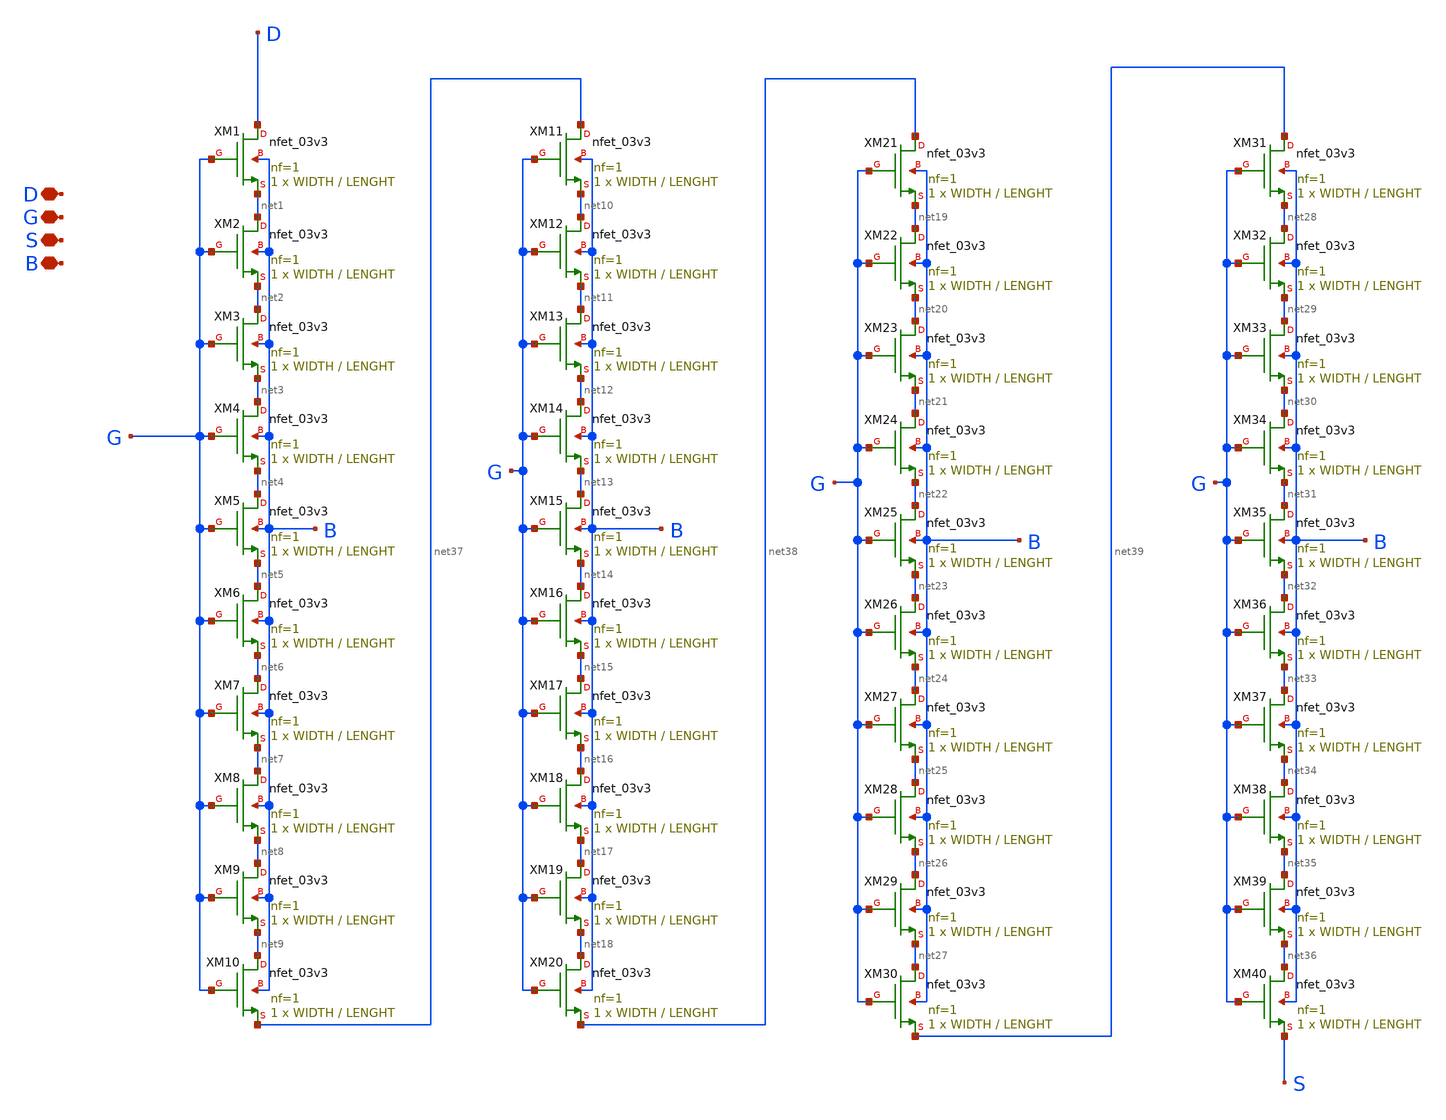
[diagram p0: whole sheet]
** sch_path: New_Extraction/Association/M4_ass.sch
**.subckt M4_ass D G S B
*.iopin D
*.iopin G
*.iopin S
*.iopin B
XM1 D G net1 B nfet_03v3 L=LENGHT W=WIDTH nf=1 ad='int((nf+1)/2) * W/nf * 0.18u' as='int((nf+2)/2) * W/nf * 0.18u'
+ pd='2*int((nf+1)/2) * (W/nf + 0.18u)' ps='2*int((nf+2)/2) * (W/nf + 0.18u)' nrd='0.18u / W' nrs='0.18u / W'
+ sa=0 sb=0 sd=0 m=1
XM2 net1 G net2 B nfet_03v3 L=LENGHT W=WIDTH nf=1 ad='int((nf+1)/2) * W/nf * 0.18u' as='int((nf+2)/2) * W/nf * 0.18u'
+ pd='2*int((nf+1)/2) * (W/nf + 0.18u)' ps='2*int((nf+2)/2) * (W/nf + 0.18u)' nrd='0.18u / W' nrs='0.18u / W'
+ sa=0 sb=0 sd=0 m=1
XM3 net2 G net3 B nfet_03v3 L=LENGHT W=WIDTH nf=1 ad='int((nf+1)/2) * W/nf * 0.18u' as='int((nf+2)/2) * W/nf * 0.18u'
+ pd='2*int((nf+1)/2) * (W/nf + 0.18u)' ps='2*int((nf+2)/2) * (W/nf + 0.18u)' nrd='0.18u / W' nrs='0.18u / W'
+ sa=0 sb=0 sd=0 m=1
XM4 net3 G net4 B nfet_03v3 L=LENGHT W=WIDTH nf=1 ad='int((nf+1)/2) * W/nf * 0.18u' as='int((nf+2)/2) * W/nf * 0.18u'
+ pd='2*int((nf+1)/2) * (W/nf + 0.18u)' ps='2*int((nf+2)/2) * (W/nf + 0.18u)' nrd='0.18u / W' nrs='0.18u / W'
+ sa=0 sb=0 sd=0 m=1
XM5 net4 G net5 B nfet_03v3 L=LENGHT W=WIDTH nf=1 ad='int((nf+1)/2) * W/nf * 0.18u' as='int((nf+2)/2) * W/nf * 0.18u'
+ pd='2*int((nf+1)/2) * (W/nf + 0.18u)' ps='2*int((nf+2)/2) * (W/nf + 0.18u)' nrd='0.18u / W' nrs='0.18u / W'
+ sa=0 sb=0 sd=0 m=1
XM6 net5 G net6 B nfet_03v3 L=LENGHT W=WIDTH nf=1 ad='int((nf+1)/2) * W/nf * 0.18u' as='int((nf+2)/2) * W/nf * 0.18u'
+ pd='2*int((nf+1)/2) * (W/nf + 0.18u)' ps='2*int((nf+2)/2) * (W/nf + 0.18u)' nrd='0.18u / W' nrs='0.18u / W'
+ sa=0 sb=0 sd=0 m=1
XM7 net6 G net7 B nfet_03v3 L=LENGHT W=WIDTH nf=1 ad='int((nf+1)/2) * W/nf * 0.18u' as='int((nf+2)/2) * W/nf * 0.18u'
+ pd='2*int((nf+1)/2) * (W/nf + 0.18u)' ps='2*int((nf+2)/2) * (W/nf + 0.18u)' nrd='0.18u / W' nrs='0.18u / W'
+ sa=0 sb=0 sd=0 m=1
XM8 net7 G net8 B nfet_03v3 L=LENGHT W=WIDTH nf=1 ad='int((nf+1)/2) * W/nf * 0.18u' as='int((nf+2)/2) * W/nf * 0.18u'
+ pd='2*int((nf+1)/2) * (W/nf + 0.18u)' ps='2*int((nf+2)/2) * (W/nf + 0.18u)' nrd='0.18u / W' nrs='0.18u / W'
+ sa=0 sb=0 sd=0 m=1
XM9 net8 G net9 B nfet_03v3 L=LENGHT W=WIDTH nf=1 ad='int((nf+1)/2) * W/nf * 0.18u' as='int((nf+2)/2) * W/nf * 0.18u'
+ pd='2*int((nf+1)/2) * (W/nf + 0.18u)' ps='2*int((nf+2)/2) * (W/nf + 0.18u)' nrd='0.18u / W' nrs='0.18u / W'
+ sa=0 sb=0 sd=0 m=1
XM10 net9 G net37 B nfet_03v3 L=LENGHT W=WIDTH nf=1 ad='int((nf+1)/2) * W/nf * 0.18u' as='int((nf+2)/2) * W/nf * 0.18u'
+ pd='2*int((nf+1)/2) * (W/nf + 0.18u)' ps='2*int((nf+2)/2) * (W/nf + 0.18u)' nrd='0.18u / W' nrs='0.18u / W'
+ sa=0 sb=0 sd=0 m=1
XM11 net37 G net10 B nfet_03v3 L=LENGHT W=WIDTH nf=1 ad='int((nf+1)/2) * W/nf * 0.18u' as='int((nf+2)/2) * W/nf * 0.18u'
+ pd='2*int((nf+1)/2) * (W/nf + 0.18u)' ps='2*int((nf+2)/2) * (W/nf + 0.18u)' nrd='0.18u / W' nrs='0.18u / W'
+ sa=0 sb=0 sd=0 m=1
XM12 net10 G net11 B nfet_03v3 L=LENGHT W=WIDTH nf=1 ad='int((nf+1)/2) * W/nf * 0.18u' as='int((nf+2)/2) * W/nf * 0.18u'
+ pd='2*int((nf+1)/2) * (W/nf + 0.18u)' ps='2*int((nf+2)/2) * (W/nf + 0.18u)' nrd='0.18u / W' nrs='0.18u / W'
+ sa=0 sb=0 sd=0 m=1
XM13 net11 G net12 B nfet_03v3 L=LENGHT W=WIDTH nf=1 ad='int((nf+1)/2) * W/nf * 0.18u' as='int((nf+2)/2) * W/nf * 0.18u'
+ pd='2*int((nf+1)/2) * (W/nf + 0.18u)' ps='2*int((nf+2)/2) * (W/nf + 0.18u)' nrd='0.18u / W' nrs='0.18u / W'
+ sa=0 sb=0 sd=0 m=1
XM14 net12 G net13 B nfet_03v3 L=LENGHT W=WIDTH nf=1 ad='int((nf+1)/2) * W/nf * 0.18u' as='int((nf+2)/2) * W/nf * 0.18u'
+ pd='2*int((nf+1)/2) * (W/nf + 0.18u)' ps='2*int((nf+2)/2) * (W/nf + 0.18u)' nrd='0.18u / W' nrs='0.18u / W'
+ sa=0 sb=0 sd=0 m=1
XM15 net13 G net14 B nfet_03v3 L=LENGHT W=WIDTH nf=1 ad='int((nf+1)/2) * W/nf * 0.18u' as='int((nf+2)/2) * W/nf * 0.18u'
+ pd='2*int((nf+1)/2) * (W/nf + 0.18u)' ps='2*int((nf+2)/2) * (W/nf + 0.18u)' nrd='0.18u / W' nrs='0.18u / W'
+ sa=0 sb=0 sd=0 m=1
XM16 net14 G net15 B nfet_03v3 L=LENGHT W=WIDTH nf=1 ad='int((nf+1)/2) * W/nf * 0.18u' as='int((nf+2)/2) * W/nf * 0.18u'
+ pd='2*int((nf+1)/2) * (W/nf + 0.18u)' ps='2*int((nf+2)/2) * (W/nf + 0.18u)' nrd='0.18u / W' nrs='0.18u / W'
+ sa=0 sb=0 sd=0 m=1
XM17 net15 G net16 B nfet_03v3 L=LENGHT W=WIDTH nf=1 ad='int((nf+1)/2) * W/nf * 0.18u' as='int((nf+2)/2) * W/nf * 0.18u'
+ pd='2*int((nf+1)/2) * (W/nf + 0.18u)' ps='2*int((nf+2)/2) * (W/nf + 0.18u)' nrd='0.18u / W' nrs='0.18u / W'
+ sa=0 sb=0 sd=0 m=1
XM18 net16 G net17 B nfet_03v3 L=LENGHT W=WIDTH nf=1 ad='int((nf+1)/2) * W/nf * 0.18u' as='int((nf+2)/2) * W/nf * 0.18u'
+ pd='2*int((nf+1)/2) * (W/nf + 0.18u)' ps='2*int((nf+2)/2) * (W/nf + 0.18u)' nrd='0.18u / W' nrs='0.18u / W'
+ sa=0 sb=0 sd=0 m=1
XM19 net17 G net18 B nfet_03v3 L=LENGHT W=WIDTH nf=1 ad='int((nf+1)/2) * W/nf * 0.18u' as='int((nf+2)/2) * W/nf * 0.18u'
+ pd='2*int((nf+1)/2) * (W/nf + 0.18u)' ps='2*int((nf+2)/2) * (W/nf + 0.18u)' nrd='0.18u / W' nrs='0.18u / W'
+ sa=0 sb=0 sd=0 m=1
XM20 net18 G net38 B nfet_03v3 L=LENGHT W=WIDTH nf=1 ad='int((nf+1)/2) * W/nf * 0.18u' as='int((nf+2)/2) * W/nf * 0.18u'
+ pd='2*int((nf+1)/2) * (W/nf + 0.18u)' ps='2*int((nf+2)/2) * (W/nf + 0.18u)' nrd='0.18u / W' nrs='0.18u / W'
+ sa=0 sb=0 sd=0 m=1
XM21 net38 G net19 B nfet_03v3 L=LENGHT W=WIDTH nf=1 ad='int((nf+1)/2) * W/nf * 0.18u' as='int((nf+2)/2) * W/nf * 0.18u'
+ pd='2*int((nf+1)/2) * (W/nf + 0.18u)' ps='2*int((nf+2)/2) * (W/nf + 0.18u)' nrd='0.18u / W' nrs='0.18u / W'
+ sa=0 sb=0 sd=0 m=1
XM22 net19 G net20 B nfet_03v3 L=LENGHT W=WIDTH nf=1 ad='int((nf+1)/2) * W/nf * 0.18u' as='int((nf+2)/2) * W/nf * 0.18u'
+ pd='2*int((nf+1)/2) * (W/nf + 0.18u)' ps='2*int((nf+2)/2) * (W/nf + 0.18u)' nrd='0.18u / W' nrs='0.18u / W'
+ sa=0 sb=0 sd=0 m=1
XM23 net20 G net21 B nfet_03v3 L=LENGHT W=WIDTH nf=1 ad='int((nf+1)/2) * W/nf * 0.18u' as='int((nf+2)/2) * W/nf * 0.18u'
+ pd='2*int((nf+1)/2) * (W/nf + 0.18u)' ps='2*int((nf+2)/2) * (W/nf + 0.18u)' nrd='0.18u / W' nrs='0.18u / W'
+ sa=0 sb=0 sd=0 m=1
XM24 net21 G net22 B nfet_03v3 L=LENGHT W=WIDTH nf=1 ad='int((nf+1)/2) * W/nf * 0.18u' as='int((nf+2)/2) * W/nf * 0.18u'
+ pd='2*int((nf+1)/2) * (W/nf + 0.18u)' ps='2*int((nf+2)/2) * (W/nf + 0.18u)' nrd='0.18u / W' nrs='0.18u / W'
+ sa=0 sb=0 sd=0 m=1
XM25 net22 G net23 B nfet_03v3 L=LENGHT W=WIDTH nf=1 ad='int((nf+1)/2) * W/nf * 0.18u' as='int((nf+2)/2) * W/nf * 0.18u'
+ pd='2*int((nf+1)/2) * (W/nf + 0.18u)' ps='2*int((nf+2)/2) * (W/nf + 0.18u)' nrd='0.18u / W' nrs='0.18u / W'
+ sa=0 sb=0 sd=0 m=1
XM26 net23 G net24 B nfet_03v3 L=LENGHT W=WIDTH nf=1 ad='int((nf+1)/2) * W/nf * 0.18u' as='int((nf+2)/2) * W/nf * 0.18u'
+ pd='2*int((nf+1)/2) * (W/nf + 0.18u)' ps='2*int((nf+2)/2) * (W/nf + 0.18u)' nrd='0.18u / W' nrs='0.18u / W'
+ sa=0 sb=0 sd=0 m=1
XM27 net24 G net25 B nfet_03v3 L=LENGHT W=WIDTH nf=1 ad='int((nf+1)/2) * W/nf * 0.18u' as='int((nf+2)/2) * W/nf * 0.18u'
+ pd='2*int((nf+1)/2) * (W/nf + 0.18u)' ps='2*int((nf+2)/2) * (W/nf + 0.18u)' nrd='0.18u / W' nrs='0.18u / W'
+ sa=0 sb=0 sd=0 m=1
XM28 net25 G net26 B nfet_03v3 L=LENGHT W=WIDTH nf=1 ad='int((nf+1)/2) * W/nf * 0.18u' as='int((nf+2)/2) * W/nf * 0.18u'
+ pd='2*int((nf+1)/2) * (W/nf + 0.18u)' ps='2*int((nf+2)/2) * (W/nf + 0.18u)' nrd='0.18u / W' nrs='0.18u / W'
+ sa=0 sb=0 sd=0 m=1
XM29 net26 G net27 B nfet_03v3 L=LENGHT W=WIDTH nf=1 ad='int((nf+1)/2) * W/nf * 0.18u' as='int((nf+2)/2) * W/nf * 0.18u'
+ pd='2*int((nf+1)/2) * (W/nf + 0.18u)' ps='2*int((nf+2)/2) * (W/nf + 0.18u)' nrd='0.18u / W' nrs='0.18u / W'
+ sa=0 sb=0 sd=0 m=1
XM30 net27 G net39 B nfet_03v3 L=LENGHT W=WIDTH nf=1 ad='int((nf+1)/2) * W/nf * 0.18u' as='int((nf+2)/2) * W/nf * 0.18u'
+ pd='2*int((nf+1)/2) * (W/nf + 0.18u)' ps='2*int((nf+2)/2) * (W/nf + 0.18u)' nrd='0.18u / W' nrs='0.18u / W'
+ sa=0 sb=0 sd=0 m=1
XM31 net39 G net28 B nfet_03v3 L=LENGHT W=WIDTH nf=1 ad='int((nf+1)/2) * W/nf * 0.18u' as='int((nf+2)/2) * W/nf * 0.18u'
+ pd='2*int((nf+1)/2) * (W/nf + 0.18u)' ps='2*int((nf+2)/2) * (W/nf + 0.18u)' nrd='0.18u / W' nrs='0.18u / W'
+ sa=0 sb=0 sd=0 m=1
XM32 net28 G net29 B nfet_03v3 L=LENGHT W=WIDTH nf=1 ad='int((nf+1)/2) * W/nf * 0.18u' as='int((nf+2)/2) * W/nf * 0.18u'
+ pd='2*int((nf+1)/2) * (W/nf + 0.18u)' ps='2*int((nf+2)/2) * (W/nf + 0.18u)' nrd='0.18u / W' nrs='0.18u / W'
+ sa=0 sb=0 sd=0 m=1
XM33 net29 G net30 B nfet_03v3 L=LENGHT W=WIDTH nf=1 ad='int((nf+1)/2) * W/nf * 0.18u' as='int((nf+2)/2) * W/nf * 0.18u'
+ pd='2*int((nf+1)/2) * (W/nf + 0.18u)' ps='2*int((nf+2)/2) * (W/nf + 0.18u)' nrd='0.18u / W' nrs='0.18u / W'
+ sa=0 sb=0 sd=0 m=1
XM34 net30 G net31 B nfet_03v3 L=LENGHT W=WIDTH nf=1 ad='int((nf+1)/2) * W/nf * 0.18u' as='int((nf+2)/2) * W/nf * 0.18u'
+ pd='2*int((nf+1)/2) * (W/nf + 0.18u)' ps='2*int((nf+2)/2) * (W/nf + 0.18u)' nrd='0.18u / W' nrs='0.18u / W'
+ sa=0 sb=0 sd=0 m=1
XM35 net31 G net32 B nfet_03v3 L=LENGHT W=WIDTH nf=1 ad='int((nf+1)/2) * W/nf * 0.18u' as='int((nf+2)/2) * W/nf * 0.18u'
+ pd='2*int((nf+1)/2) * (W/nf + 0.18u)' ps='2*int((nf+2)/2) * (W/nf + 0.18u)' nrd='0.18u / W' nrs='0.18u / W'
+ sa=0 sb=0 sd=0 m=1
XM36 net32 G net33 B nfet_03v3 L=LENGHT W=WIDTH nf=1 ad='int((nf+1)/2) * W/nf * 0.18u' as='int((nf+2)/2) * W/nf * 0.18u'
+ pd='2*int((nf+1)/2) * (W/nf + 0.18u)' ps='2*int((nf+2)/2) * (W/nf + 0.18u)' nrd='0.18u / W' nrs='0.18u / W'
+ sa=0 sb=0 sd=0 m=1
XM37 net33 G net34 B nfet_03v3 L=LENGHT W=WIDTH nf=1 ad='int((nf+1)/2) * W/nf * 0.18u' as='int((nf+2)/2) * W/nf * 0.18u'
+ pd='2*int((nf+1)/2) * (W/nf + 0.18u)' ps='2*int((nf+2)/2) * (W/nf + 0.18u)' nrd='0.18u / W' nrs='0.18u / W'
+ sa=0 sb=0 sd=0 m=1
XM38 net34 G net35 B nfet_03v3 L=LENGHT W=WIDTH nf=1 ad='int((nf+1)/2) * W/nf * 0.18u' as='int((nf+2)/2) * W/nf * 0.18u'
+ pd='2*int((nf+1)/2) * (W/nf + 0.18u)' ps='2*int((nf+2)/2) * (W/nf + 0.18u)' nrd='0.18u / W' nrs='0.18u / W'
+ sa=0 sb=0 sd=0 m=1
XM39 net35 G net36 B nfet_03v3 L=LENGHT W=WIDTH nf=1 ad='int((nf+1)/2) * W/nf * 0.18u' as='int((nf+2)/2) * W/nf * 0.18u'
+ pd='2*int((nf+1)/2) * (W/nf + 0.18u)' ps='2*int((nf+2)/2) * (W/nf + 0.18u)' nrd='0.18u / W' nrs='0.18u / W'
+ sa=0 sb=0 sd=0 m=1
XM40 net36 G S B nfet_03v3 L=LENGHT W=WIDTH nf=1 ad='int((nf+1)/2) * W/nf * 0.18u' as='int((nf+2)/2) * W/nf * 0.18u'
+ pd='2*int((nf+1)/2) * (W/nf + 0.18u)' ps='2*int((nf+2)/2) * (W/nf + 0.18u)' nrd='0.18u / W' nrs='0.18u / W'
+ sa=0 sb=0 sd=0 m=1
**.ends
.end
